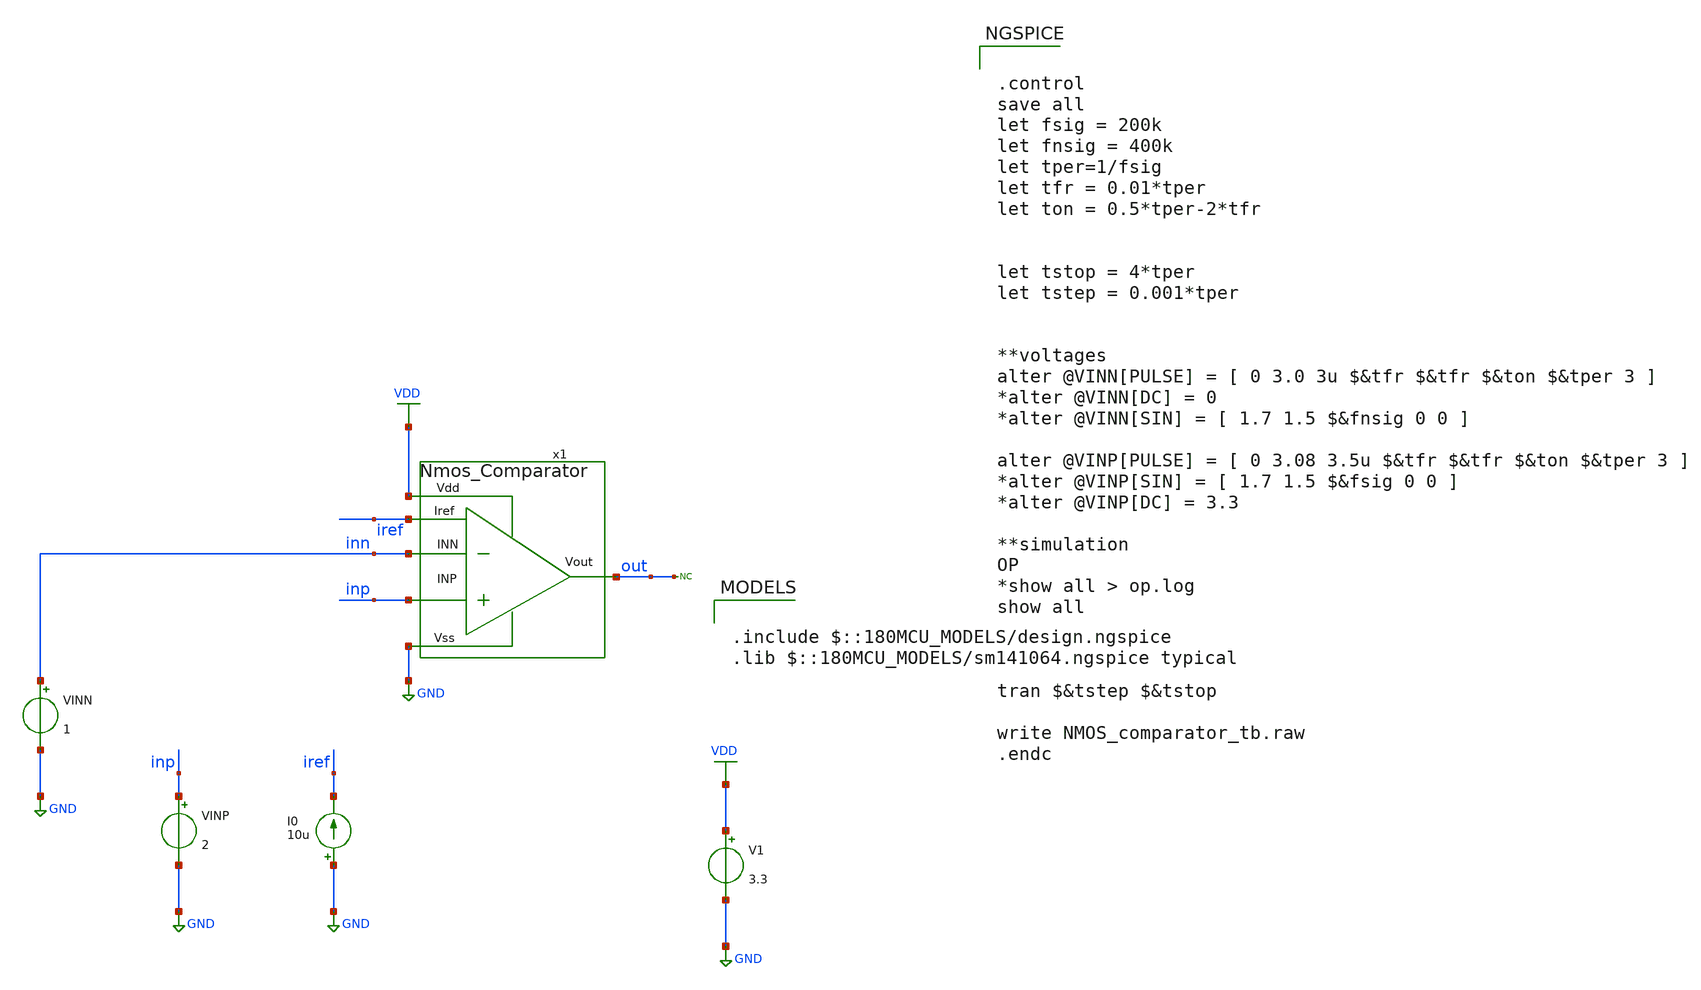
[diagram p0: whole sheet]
** sch_path: designs/libs/tb_analog/Comparator/NMOS_comparator_tb.sch
**.subckt NMOS_comparator_tb
I0 GND iref 10u
V1 VDD GND 3.3
VINP inp GND 2
* noconn out
VINN inn GND 1
x1 VDD out inn inp iref GND Nmos_Comparator
**** begin user architecture code


.control
save all
let fsig = 200k
let fnsig = 400k
let tper=1/fsig
let tfr = 0.01*tper
let ton = 0.5*tper-2*tfr


let tstop = 4*tper
let tstep = 0.001*tper


**voltages
alter @VINN[PULSE] = [ 0 3.0 3u $&tfr $&tfr $&ton $&tper 3 ]
*alter @VINN[DC] = 0
*alter @VINN[SIN] = [ 1.7 1.5 $&fnsig 0 0 ]

alter @VINP[PULSE] = [ 0 3.08 3.5u $&tfr $&tfr $&ton $&tper 3 ]
*alter @VINP[SIN] = [ 1.7 1.5 $&fsig 0 0 ]
*alter @VINP[DC] = 3.3

**simulation
OP
*show all > op.log
show all



tran $&tstep $&tstop

write NMOS_comparator_tb.raw
.endc



.include $::180MCU_MODELS/design.ngspice
.lib $::180MCU_MODELS/sm141064.ngspice typical

**** end user architecture code
**.ends

* expanding   symbol:  libs/core_analog/Comparator/Nmos_Comparator.sym # of pins=6
** sym_path: designs/libs/core_analog/Comparator/Nmos_Comparator.sym
** sch_path: designs/libs/core_analog/Comparator/Nmos_Comparator.sch
.subckt Nmos_Comparator Vdd Vout INN INP Iref Vss
*.ipin Vss
*.ipin Vdd
*.ipin Iref
*.ipin INN
*.ipin INP
*.opin Vout
XM3 net1 net1 Vss Vss nfet_03v3 L=1u W=3.56u nf=1 ad='int((nf+1)/2) * W/nf * 0.18u' as='int((nf+2)/2) * W/nf * 0.18u'
+ pd='2*int((nf+1)/2) * (W/nf + 0.18u)' ps='2*int((nf+2)/2) * (W/nf + 0.18u)' nrd='0.18u / W' nrs='0.18u / W'
+ sa=0 sb=0 sd=0 m=1
XM4 Vout net1 Vss Vss nfet_03v3 L=1u W=3.56u nf=1 ad='int((nf+1)/2) * W/nf * 0.18u' as='int((nf+2)/2) * W/nf * 0.18u'
+ pd='2*int((nf+1)/2) * (W/nf + 0.18u)' ps='2*int((nf+2)/2) * (W/nf + 0.18u)' nrd='0.18u / W' nrs='0.18u / W'
+ sa=0 sb=0 sd=0 m=1
XM5 net2 INN net3 Vss nfet_03v3 L=1u W=4.13u nf=1 ad='int((nf+1)/2) * W/nf * 0.18u' as='int((nf+2)/2) * W/nf * 0.18u'
+ pd='2*int((nf+1)/2) * (W/nf + 0.18u)' ps='2*int((nf+2)/2) * (W/nf + 0.18u)' nrd='0.18u / W' nrs='0.18u / W'
+ sa=0 sb=0 sd=0 m=1
XM6 net4 INP net3 Vss nfet_03v3 L=1u W=4.13u nf=1 ad='int((nf+1)/2) * W/nf * 0.18u' as='int((nf+2)/2) * W/nf * 0.18u'
+ pd='2*int((nf+1)/2) * (W/nf + 0.18u)' ps='2*int((nf+2)/2) * (W/nf + 0.18u)' nrd='0.18u / W' nrs='0.18u / W'
+ sa=0 sb=0 sd=0 m=1
XM7 net1 net2 Vdd Vdd pfet_03v3 L=0.5u W=4.1u nf=4 ad='int((nf+1)/2) * W/nf * 0.18u' as='int((nf+2)/2) * W/nf * 0.18u'
+ pd='2*int((nf+1)/2) * (W/nf + 0.18u)' ps='2*int((nf+2)/2) * (W/nf + 0.18u)' nrd='0.18u / W' nrs='0.18u / W'
+ sa=0 sb=0 sd=0 m=4
XM8 net2 net4 Vdd Vdd pfet_03v3 L=0.5u W=5u nf=4 ad='int((nf+1)/2) * W/nf * 0.18u' as='int((nf+2)/2) * W/nf * 0.18u'
+ pd='2*int((nf+1)/2) * (W/nf + 0.18u)' ps='2*int((nf+2)/2) * (W/nf + 0.18u)' nrd='0.18u / W' nrs='0.18u / W'
+ sa=0 sb=0 sd=0 m=4
XM9 net4 net4 Vdd Vdd pfet_03v3 L=0.5u W=5u nf=2 ad='int((nf+1)/2) * W/nf * 0.18u' as='int((nf+2)/2) * W/nf * 0.18u'
+ pd='2*int((nf+1)/2) * (W/nf + 0.18u)' ps='2*int((nf+2)/2) * (W/nf + 0.18u)' nrd='0.18u / W' nrs='0.18u / W'
+ sa=0 sb=0 sd=0 m=2
XM10 net4 net2 Vdd Vdd pfet_03v3 L=0.5u W=5u nf=4 ad='int((nf+1)/2) * W/nf * 0.18u' as='int((nf+2)/2) * W/nf * 0.18u'
+ pd='2*int((nf+1)/2) * (W/nf + 0.18u)' ps='2*int((nf+2)/2) * (W/nf + 0.18u)' nrd='0.18u / W' nrs='0.18u / W'
+ sa=0 sb=0 sd=0 m=4
XM11 net2 net2 Vdd Vdd pfet_03v3 L=0.5u W=5u nf=2 ad='int((nf+1)/2) * W/nf * 0.18u' as='int((nf+2)/2) * W/nf * 0.18u'
+ pd='2*int((nf+1)/2) * (W/nf + 0.18u)' ps='2*int((nf+2)/2) * (W/nf + 0.18u)' nrd='0.18u / W' nrs='0.18u / W'
+ sa=0 sb=0 sd=0 m=2
XM12 Vout net4 Vdd Vdd pfet_03v3 L=0.5u W=4.1u nf=4 ad='int((nf+1)/2) * W/nf * 0.18u' as='int((nf+2)/2) * W/nf * 0.18u'
+ pd='2*int((nf+1)/2) * (W/nf + 0.18u)' ps='2*int((nf+2)/2) * (W/nf + 0.18u)' nrd='0.18u / W' nrs='0.18u / W'
+ sa=0 sb=0 sd=0 m=4
x1 Iref Vss Iref Vss unit_nmos M=1
x2 net3 Vss Iref Vss unit_nmos M=2
.ends


* expanding   symbol:  libs/core_analog/unit_nmos/unit_nmos.sym # of pins=4
** sym_path: libs/core_analog/unit_nmos/unit_nmos.sym
** sch_path: libs/core_analog/unit_nmos/unit_nmos.sch
.subckt unit_nmos drain sub gate source
*.iopin drain
*.iopin source
*.iopin sub
*.iopin gate
XM1 drain gate source sub nfet_03v3 L=1u W=2.5u nf=1 ad='int((nf+1)/2) * W/nf * 0.18u' as='int((nf+2)/2) * W/nf * 0.18u'
+ pd='2*int((nf+1)/2) * (W/nf + 0.18u)' ps='2*int((nf+2)/2) * (W/nf + 0.18u)' nrd='0.18u / W' nrs='0.18u / W'
+ sa=0 sb=0 sd=0 m={M}
**** begin user architecture code

.param M=1

**** end user architecture code
.ends

.GLOBAL GND
.GLOBAL VDD
.end
